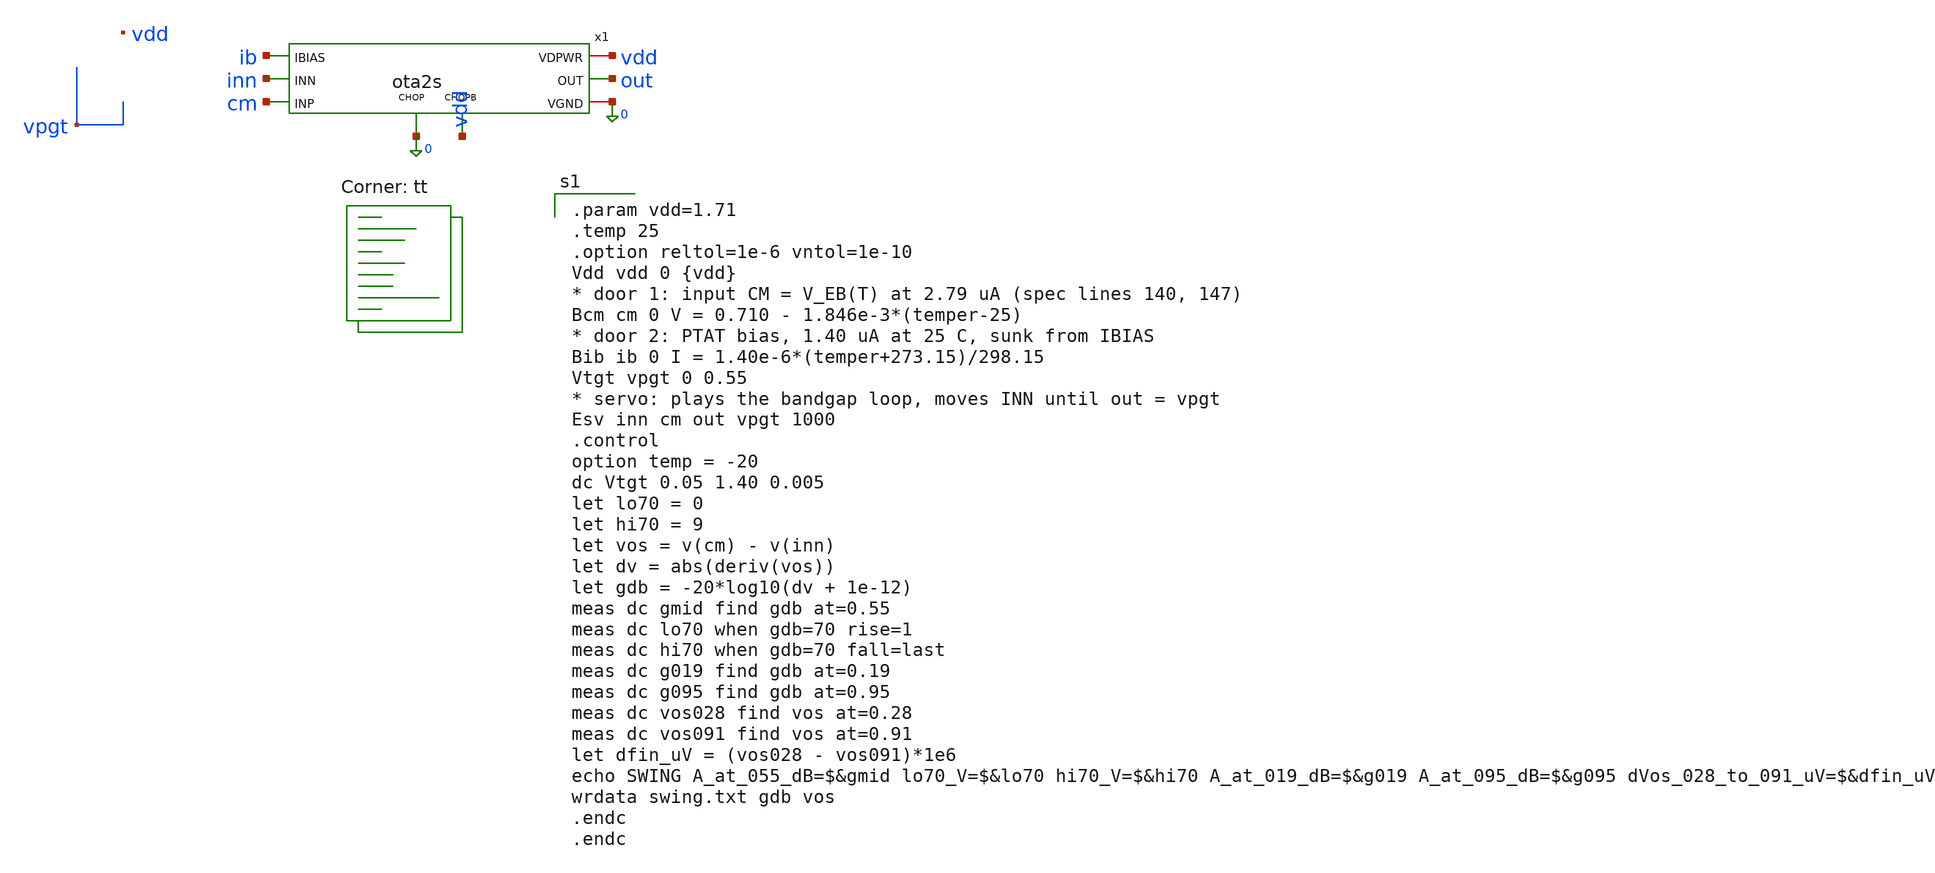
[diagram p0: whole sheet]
** sch_path: xschem/tb_ota2s_swing.sch
**.subckt tb_ota2s_swing
x1 cm inn out vdd 0 ib 0 vdd ota2s
**** begin user architecture code
.lib $::SKYWATER_MODELS/sky130.lib.spice tt

.param vdd=1.71
.temp 25
.option reltol=1e-6 vntol=1e-10
Vdd vdd 0 {vdd}
* door 1: input CM = V_EB(T) at 2.79 uA (spec lines 140, 147)
Bcm cm 0 V = 0.710 - 1.846e-3*(temper-25)
* door 2: PTAT bias, 1.40 uA at 25 C, sunk from IBIAS
Bib ib 0 I = 1.40e-6*(temper+273.15)/298.15
Vtgt vpgt 0 0.55
* servo: plays the bandgap loop, moves INN until out = vpgt
Esv inn cm out vpgt 1000
.control
option temp = -20
dc Vtgt 0.05 1.40 0.005
let lo70 = 0
let hi70 = 9
let vos = v(cm) - v(inn)
let dv = abs(deriv(vos))
let gdb = -20*log10(dv + 1e-12)
meas dc gmid find gdb at=0.55
meas dc lo70 when gdb=70 rise=1
meas dc hi70 when gdb=70 fall=last
meas dc g019 find gdb at=0.19
meas dc g095 find gdb at=0.95
meas dc vos028 find vos at=0.28
meas dc vos091 find vos at=0.91
let dfin_uV = (vos028 - vos091)*1e6
echo SWING A_at_055_dB=$&gmid lo70_V=$&lo70 hi70_V=$&hi70 A_at_019_dB=$&g019 A_at_095_dB=$&g095
+ dVos_028_to_091_uV=$&dfin_uV
wrdata swing.txt gdb vos
.endc
.endc

**** end user architecture code
**.ends

* expanding   symbol:  ota2s.sym # of pins=8
** sym_path: xschem/ota2s.sym
** sch_path: xschem/ota2s.sch
.subckt ota2s INP INN OUT VDPWR VGND IBIAS CHOP CHOPB
*.ipin INN
*.ipin INP
*.ipin IBIAS
*.opin OUT
*.iopin VDPWR
*.iopin VGND
*.ipin CHOPB
*.ipin CHOP
XMREF IBIAS IBIAS VDPWR VDPWR sky130_fd_pr__pfet_01v8 L=4 W=20 nf=1 ad='int((1 + 1)/2) * 20 / 1 * 0.29'
+ as='int((1 + 2)/2) * 20 / 1 * 0.29' pd='2*int((1 + 1)/2) * (20 / 1 + 0.29)' ps='2*int((1 + 2)/2) * (20 / 1 + 0.29)'
+ nrd='0.29 / 20 ' nrs='0.29 / 20 ' sa=0 sb=0 sd=0 mult=1 m=1
XMTAIL tail IBIAS VDPWR VDPWR sky130_fd_pr__pfet_01v8 L=4 W=20 nf=1 ad='int((1 + 1)/2) * 20 / 1 * 0.29'
+ as='int((1 + 2)/2) * 20 / 1 * 0.29' pd='2*int((1 + 1)/2) * (20 / 1 + 0.29)' ps='2*int((1 + 2)/2) * (20 / 1 + 0.29)'
+ nrd='0.29 / 20 ' nrs='0.29 / 20 ' sa=0 sb=0 sd=0 mult=2 m=2
XMP1 d1 INN tail VDPWR sky130_fd_pr__pfet_01v8_lvt L=6 W=25 nf=1 ad='int((1 + 1)/2) * 25 / 1 * 0.29'
+ as='int((1 + 2)/2) * 25 / 1 * 0.29' pd='2*int((1 + 1)/2) * (25 / 1 + 0.29)' ps='2*int((1 + 2)/2) * (25 / 1 + 0.29)'
+ nrd='0.29 / 25 ' nrs='0.29 / 25 ' sa=0 sb=0 sd=0 mult=24 m=24
XMP2 x1 INP tail VDPWR sky130_fd_pr__pfet_01v8_lvt L=6 W=25 nf=1 ad='int((1 + 1)/2) * 25 / 1 * 0.29'
+ as='int((1 + 2)/2) * 25 / 1 * 0.29' pd='2*int((1 + 1)/2) * (25 / 1 + 0.29)' ps='2*int((1 + 2)/2) * (25 / 1 + 0.29)'
+ nrd='0.29 / 25 ' nrs='0.29 / 25 ' sa=0 sb=0 sd=0 mult=24 m=24
XMN1 d1 g12 VGND VGND sky130_fd_pr__nfet_01v8 L=20 W=6 nf=1 ad='int((1 + 1)/2) * 6 / 1 * 0.29' as='int((1 + 2)/2) * 6 / 1 * 0.29'
+ pd='2*int((1 + 1)/2) * (6 / 1 + 0.29)' ps='2*int((1 + 2)/2) * (6 / 1 + 0.29)' nrd='0.29 / 6 ' nrs='0.29 / 6 '
+ sa=0 sb=0 sd=0 mult=2 m=2
XMN2 x1 g12 VGND VGND sky130_fd_pr__nfet_01v8 L=20 W=6 nf=1 ad='int((1 + 1)/2) * 6 / 1 * 0.29' as='int((1 + 2)/2) * 6 / 1 * 0.29'
+ pd='2*int((1 + 1)/2) * (6 / 1 + 0.29)' ps='2*int((1 + 2)/2) * (6 / 1 + 0.29)' nrd='0.29 / 6 ' nrs='0.29 / 6 '
+ sa=0 sb=0 sd=0 mult=2 m=2
XMP3 OUT IBIAS VDPWR VDPWR sky130_fd_pr__pfet_01v8 L=4 W=20 nf=1 ad='int((1 + 1)/2) * 20 / 1 * 0.29'
+ as='int((1 + 2)/2) * 20 / 1 * 0.29' pd='2*int((1 + 1)/2) * (20 / 1 + 0.29)' ps='2*int((1 + 2)/2) * (20 / 1 + 0.29)'
+ nrd='0.29 / 20 ' nrs='0.29 / 20 ' sa=0 sb=0 sd=0 mult=6 m=6
XMN3 OUT g3 VGND VGND sky130_fd_pr__nfet_01v8 L=1 W=7 nf=1 ad='int((1 + 1)/2) * 7 / 1 * 0.29' as='int((1 + 2)/2) * 7 / 1 * 0.29'
+ pd='2*int((1 + 1)/2) * (7 / 1 + 0.29)' ps='2*int((1 + 2)/2) * (7 / 1 + 0.29)' nrd='0.29 / 7 ' nrs='0.29 / 7 '
+ sa=0 sb=0 sd=0 mult=1 m=1
XRZ1 net1 g3 VGND sky130_fd_pr__res_high_po_1p41 L=20 mult=1 m=1
XRZ2 net2 net1 VGND sky130_fd_pr__res_high_po_1p41 L=20 mult=1 m=1
XRZ3 net3 net2 VGND sky130_fd_pr__res_high_po_1p41 L=20 mult=1 m=1
XRZ4 net4 net3 VGND sky130_fd_pr__res_high_po_1p41 L=20 mult=1 m=1
XRZ5 net5 net4 VGND sky130_fd_pr__res_high_po_1p41 L=20 mult=1 m=1
XRZ6 cz net5 VGND sky130_fd_pr__res_high_po_1p41 L=20 mult=1 m=1
XCC cz OUT sky130_fd_pr__cap_mim_m3_1 W=25 L=25 MF=8 m=8
XDP tail VDPWR tail VDPWR sky130_fd_pr__pfet_01v8_lvt L=6 W=25 nf=1 ad='int((1 + 1)/2) * 25 / 1 * 0.29'
+ as='int((1 + 2)/2) * 25 / 1 * 0.29' pd='2*int((1 + 1)/2) * (25 / 1 + 0.29)' ps='2*int((1 + 2)/2) * (25 / 1 + 0.29)'
+ nrd='0.29 / 25 ' nrs='0.29 / 25 ' sa=0 sb=0 sd=0 mult=8 m=8
XDNA d1 VGND VGND VGND sky130_fd_pr__nfet_01v8 L=20 W=6 nf=1 ad='int((1 + 1)/2) * 6 / 1 * 0.29' as='int((1 + 2)/2) * 6 / 1 * 0.29'
+ pd='2*int((1 + 1)/2) * (6 / 1 + 0.29)' ps='2*int((1 + 2)/2) * (6 / 1 + 0.29)' nrd='0.29 / 6 ' nrs='0.29 / 6 '
+ sa=0 sb=0 sd=0 mult=2 m=2
XDNB x1 VGND VGND VGND sky130_fd_pr__nfet_01v8 L=20 W=6 nf=1 ad='int((1 + 1)/2) * 6 / 1 * 0.29' as='int((1 + 2)/2) * 6 / 1 * 0.29'
+ pd='2*int((1 + 1)/2) * (6 / 1 + 0.29)' ps='2*int((1 + 2)/2) * (6 / 1 + 0.29)' nrd='0.29 / 6 ' nrs='0.29 / 6 '
+ sa=0 sb=0 sd=0 mult=2 m=2
XDB VDPWR VDPWR VDPWR VDPWR sky130_fd_pr__pfet_01v8 L=4 W=20 nf=1 ad='int((1 + 1)/2) * 20 / 1 * 0.29'
+ as='int((1 + 2)/2) * 20 / 1 * 0.29' pd='2*int((1 + 1)/2) * (20 / 1 + 0.29)' ps='2*int((1 + 2)/2) * (20 / 1 + 0.29)'
+ nrd='0.29 / 20 ' nrs='0.29 / 20 ' sa=0 sb=0 sd=0 mult=2 m=2
XRD1 VGND VGND VGND sky130_fd_pr__res_high_po_1p41 L=20 mult=1 m=1
XRD2 VGND VGND VGND sky130_fd_pr__res_high_po_1p41 L=20 mult=1 m=1
XSD1 d1 CHOPB g12 VGND sky130_fd_pr__nfet_01v8 L=0.5 W=6 nf=1 ad='int((1 + 1)/2) * 6 / 1 * 0.29' as='int((1 + 2)/2) * 6 / 1 * 0.29'
+ pd='2*int((1 + 1)/2) * (6 / 1 + 0.29)' ps='2*int((1 + 2)/2) * (6 / 1 + 0.29)' nrd='0.29 / 6 ' nrs='0.29 / 6 '
+ sa=0 sb=0 sd=0 mult=1 m=1
XSD2 x1 CHOP g12 VGND sky130_fd_pr__nfet_01v8 L=0.5 W=6 nf=1 ad='int((1 + 1)/2) * 6 / 1 * 0.29' as='int((1 + 2)/2) * 6 / 1 * 0.29'
+ pd='2*int((1 + 1)/2) * (6 / 1 + 0.29)' ps='2*int((1 + 2)/2) * (6 / 1 + 0.29)' nrd='0.29 / 6 ' nrs='0.29 / 6 '
+ sa=0 sb=0 sd=0 mult=1 m=1
XSG2 g3 CHOP d1 VGND sky130_fd_pr__nfet_01v8 L=0.5 W=6 nf=1 ad='int((1 + 1)/2) * 6 / 1 * 0.29' as='int((1 + 2)/2) * 6 / 1 * 0.29'
+ pd='2*int((1 + 1)/2) * (6 / 1 + 0.29)' ps='2*int((1 + 2)/2) * (6 / 1 + 0.29)' nrd='0.29 / 6 ' nrs='0.29 / 6 '
+ sa=0 sb=0 sd=0 mult=1 m=1
XSG1 x1 CHOPB g3 VGND sky130_fd_pr__nfet_01v8 L=0.5 W=6 nf=1 ad='int((1 + 1)/2) * 6 / 1 * 0.29' as='int((1 + 2)/2) * 6 / 1 * 0.29'
+ pd='2*int((1 + 1)/2) * (6 / 1 + 0.29)' ps='2*int((1 + 2)/2) * (6 / 1 + 0.29)' nrd='0.29 / 6 ' nrs='0.29 / 6 '
+ sa=0 sb=0 sd=0 mult=1 m=1
.ends

.end
